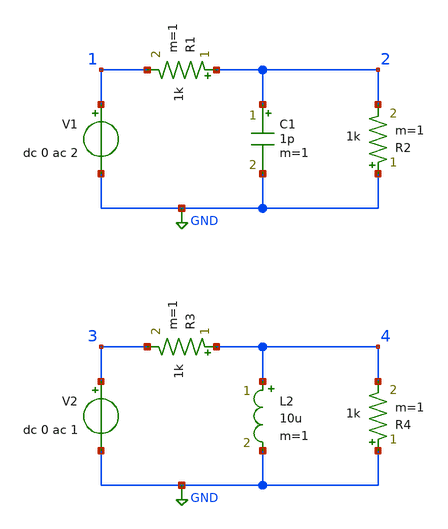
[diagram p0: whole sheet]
** sch_path: circuitos/exemplo02a.sch
**.subckt exemplo02a
C1 2 GND 1p m=1
R1 2 1 1k m=1
V1 1 GND dc 0 ac 2
R2 GND 2 1k m=1
L2 4 GND 10u m=1
R3 4 3 1k m=1
V2 3 GND dc 0 ac 1
R4 GND 4 1k m=1
**** begin user architecture code

.control
  ac lin 1001 100 10G
  plot xlog db(V(2)/v(1))
  plot xlog db(V(4)/v(3))
.endc

**** end user architecture code
**.ends
.GLOBAL GND
.end
